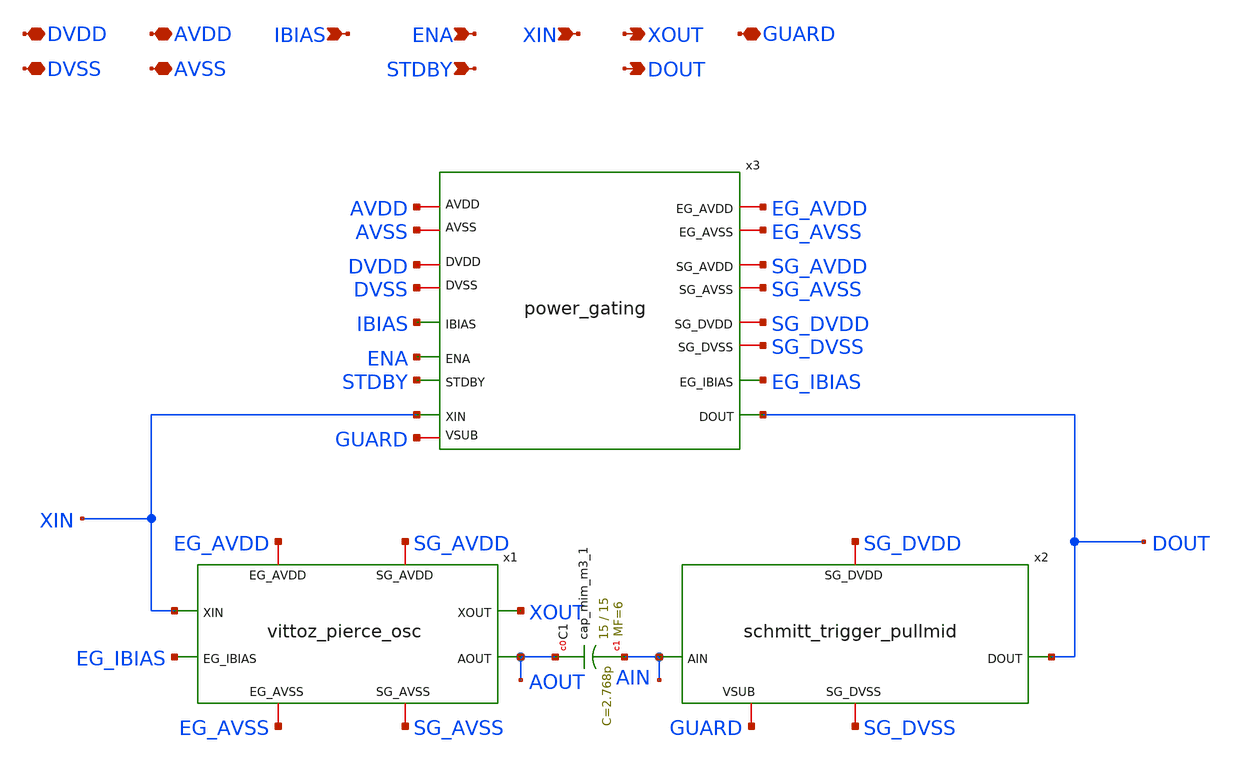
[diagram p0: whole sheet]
** sch_path: xschem/sky130_ht_ip__hsxo_cpz1.sch
**.subckt sky130_ht_ip__hsxo_cpz1 DVDD DVSS AVDD AVSS ENA STDBY XIN XOUT DOUT IBIAS GUARD
*.iopin DVDD
*.iopin DVSS
*.iopin AVDD
*.iopin AVSS
*.ipin ENA
*.ipin STDBY
*.ipin XIN
*.opin XOUT
*.opin DOUT
*.ipin IBIAS
*.iopin GUARD
x1 XOUT SG_AVDD EG_AVDD XIN EG_IBIAS AOUT SG_AVSS EG_AVSS vittoz_pierce_osc
x2 SG_DVDD AIN DOUT SG_DVSS GUARD schmitt_trigger_pullmid
XC1 AOUT AIN sky130_fd_pr__cap_mim_m3_1 W=15 L=15 MF=6 m=6
x3 DOUT SG_AVDD DVDD EG_IBIAS SG_DVDD AVDD IBIAS EG_AVDD ENA SG_DVSS SG_AVSS STDBY EG_AVSS AVSS DVSS
+ XIN GUARD power_gating
**.ends
.end
